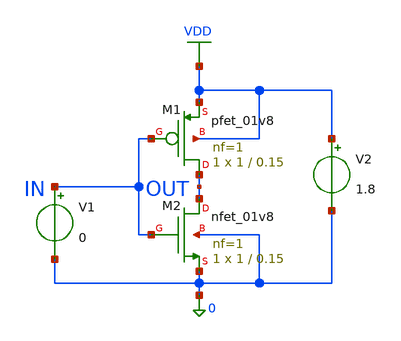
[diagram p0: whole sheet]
** sch_path: inverter.sch
**.subckt inverter
XM1 OUT IN VDD VDD sky130_fd_pr__pfet_01v8 L=0.15 W=1 nf=1 ad='int((1 + 1)/2) * 1 / 1 * 0.29' as='int((1 + 2)/2) * 1 / 1 * 0.29'
+ pd='2*int((1 + 1)/2) * (1 / 1 + 0.29)' ps='2*int((1 + 2)/2) * (1 / 1 + 0.29)' nrd='0.29 / 1 ' nrs='0.29 / 1 '
+ sa=0 sb=0 sd=0 mult=1 m=1
XM2 OUT IN 0 0 sky130_fd_pr__nfet_01v8 L=0.15 W=1 nf=1 ad='int((1 + 1)/2) * 1 / 1 * 0.29' as='int((1 + 2)/2) * 1 / 1 * 0.29'
+ pd='2*int((1 + 1)/2) * (1 / 1 + 0.29)' ps='2*int((1 + 2)/2) * (1 / 1 + 0.29)' nrd='0.29 / 1 ' nrs='0.29 / 1 '
+ sa=0 sb=0 sd=0 mult=1 m=1
V1 IN 0 0
V2 VDD 0 1.8
**.ends
.GLOBAL VDD
.end
